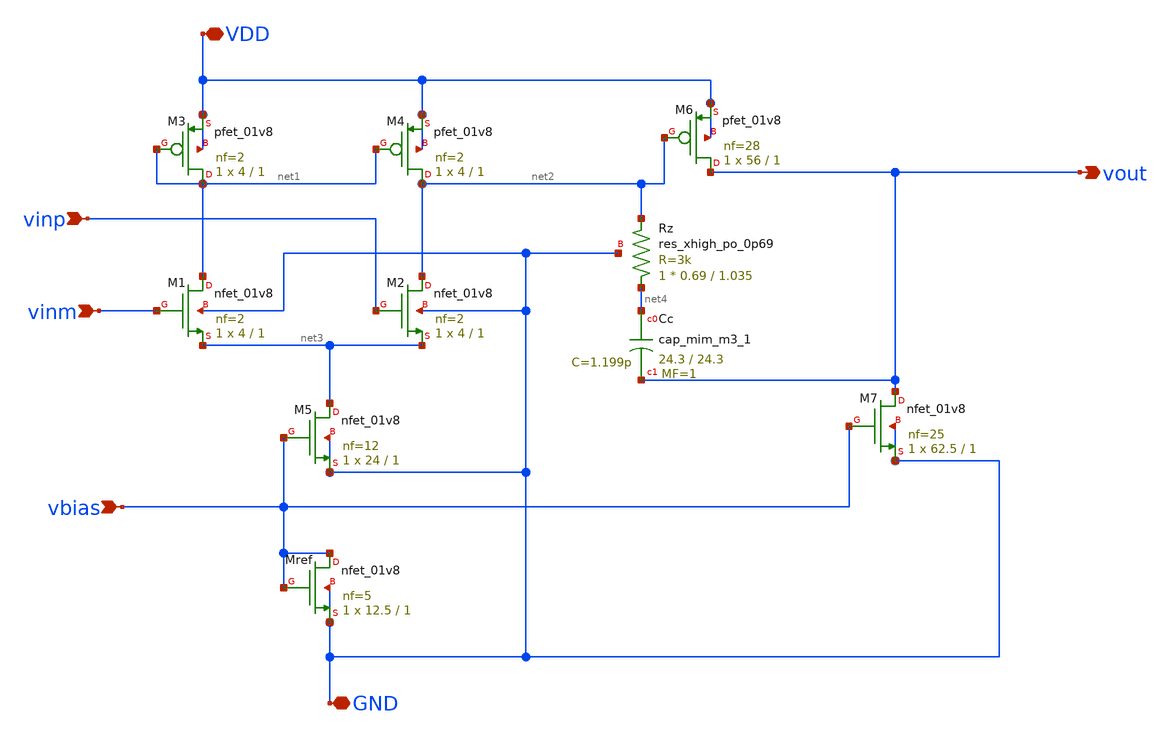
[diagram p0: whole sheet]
** sch_path: 03_sch/ota2_miller.sch
**.subckt ota2_miller GND vinp vinm vout vbias VDD
*.iopin GND
*.ipin vinp
*.ipin vinm
*.opin vout
*.ipin vbias
*.iopin VDD
XM5 net3 vbias GND GND sky130_fd_pr__nfet_01v8 L=1 W=24 nf=12 ad='int((nf+1)/2) * W/nf * 0.29' as='int((nf+2)/2) * W/nf * 0.29'
+ pd='2*int((nf+1)/2) * (W/nf + 0.29)' ps='2*int((nf+2)/2) * (W/nf + 0.29)' nrd='0.29 / W' nrs='0.29 / W'
+ sa=0 sb=0 sd=0 mult=1 m=1
XM7 vout vbias GND GND sky130_fd_pr__nfet_01v8 L=1 W=62.5 nf=25 ad='int((nf+1)/2) * W/nf * 0.29' as='int((nf+2)/2) * W/nf * 0.29'
+ pd='2*int((nf+1)/2) * (W/nf + 0.29)' ps='2*int((nf+2)/2) * (W/nf + 0.29)' nrd='0.29 / W' nrs='0.29 / W'
+ sa=0 sb=0 sd=0 mult=1 m=1
XMref vbias vbias GND GND sky130_fd_pr__nfet_01v8 L=1 W=12.5 nf=5 ad='int((nf+1)/2) * W/nf * 0.29' as='int((nf+2)/2) * W/nf * 0.29'
+ pd='2*int((nf+1)/2) * (W/nf + 0.29)' ps='2*int((nf+2)/2) * (W/nf + 0.29)' nrd='0.29 / W' nrs='0.29 / W'
+ sa=0 sb=0 sd=0 mult=1 m=1
XRz net4 net2 GND sky130_fd_pr__res_xhigh_po_0p69 L=1.035 mult=1 m=1
XCc net4 vout sky130_fd_pr__cap_mim_m3_1 W=24.3 L=24.3 MF=1 m=1
XM3 net1 net1 VDD VDD sky130_fd_pr__pfet_01v8 L=1 W=4 nf=2 ad='int((nf+1)/2) * W/nf * 0.29' as='int((nf+2)/2) * W/nf * 0.29'
+ pd='2*int((nf+1)/2) * (W/nf + 0.29)' ps='2*int((nf+2)/2) * (W/nf + 0.29)' nrd='0.29 / W' nrs='0.29 / W'
+ sa=0 sb=0 sd=0 mult=1 m=1
XM4 net2 net1 VDD VDD sky130_fd_pr__pfet_01v8 L=1 W=4 nf=2 ad='int((nf+1)/2) * W/nf * 0.29' as='int((nf+2)/2) * W/nf * 0.29'
+ pd='2*int((nf+1)/2) * (W/nf + 0.29)' ps='2*int((nf+2)/2) * (W/nf + 0.29)' nrd='0.29 / W' nrs='0.29 / W'
+ sa=0 sb=0 sd=0 mult=1 m=1
XM6 vout net2 VDD VDD sky130_fd_pr__pfet_01v8 L=1 W=56 nf=28 ad='int((nf+1)/2) * W/nf * 0.29' as='int((nf+2)/2) * W/nf * 0.29'
+ pd='2*int((nf+1)/2) * (W/nf + 0.29)' ps='2*int((nf+2)/2) * (W/nf + 0.29)' nrd='0.29 / W' nrs='0.29 / W'
+ sa=0 sb=0 sd=0 mult=1 m=1
XM1 net1 vinm net3 GND sky130_fd_pr__nfet_01v8 L=1 W=4 nf=2 ad='int((nf+1)/2) * W/nf * 0.29' as='int((nf+2)/2) * W/nf * 0.29'
+ pd='2*int((nf+1)/2) * (W/nf + 0.29)' ps='2*int((nf+2)/2) * (W/nf + 0.29)' nrd='0.29 / W' nrs='0.29 / W'
+ sa=0 sb=0 sd=0 mult=1 m=1
XM2 net2 vinp net3 GND sky130_fd_pr__nfet_01v8 L=1 W=4 nf=2 ad='int((nf+1)/2) * W/nf * 0.29' as='int((nf+2)/2) * W/nf * 0.29'
+ pd='2*int((nf+1)/2) * (W/nf + 0.29)' ps='2*int((nf+2)/2) * (W/nf + 0.29)' nrd='0.29 / W' nrs='0.29 / W'
+ sa=0 sb=0 sd=0 mult=1 m=1
**.ends
.end
